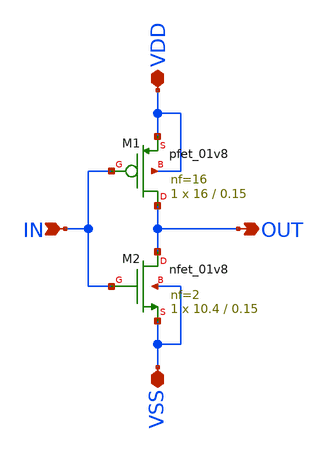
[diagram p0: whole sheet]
** sch_path: DISEÑO/ANALOGICO/V;SI/RETARDO/xschem/INV_16.sch
**.subckt INV_16 IN OUT VDD VSS
*.ipin IN
*.opin OUT
*.iopin VDD
*.iopin VSS
XM1 OUT IN VDD VDD sky130_fd_pr__pfet_01v8 L=0.15 W=16 nf=16 ad='int((nf+1)/2) * W/nf * 0.29' as='int((nf+2)/2) * W/nf * 0.29'
+ pd='2*int((nf+1)/2) * (W/nf + 0.29)' ps='2*int((nf+2)/2) * (W/nf + 0.29)' nrd='0.29 / W' nrs='0.29 / W'
+ sa=0 sb=0 sd=0 mult=1 m=1
XM2 OUT IN VSS VSS sky130_fd_pr__nfet_01v8 L=0.15 W=10.4 nf=2 ad='int((nf+1)/2) * W/nf * 0.29' as='int((nf+2)/2) * W/nf * 0.29'
+ pd='2*int((nf+1)/2) * (W/nf + 0.29)' ps='2*int((nf+2)/2) * (W/nf + 0.29)' nrd='0.29 / W' nrs='0.29 / W'
+ sa=0 sb=0 sd=0 mult=1 m=1
**.ends
.end
